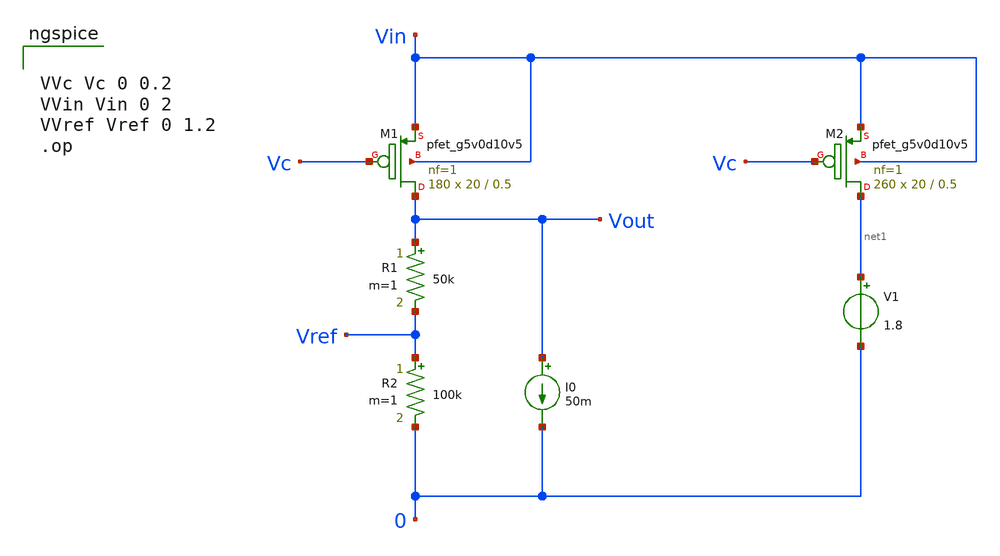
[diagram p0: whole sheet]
** sch_path: Analog_Blocks/LDO/Testbench/Pass_transistor_TB.sch
**.subckt Pass_transistor_TB
XM1 Vout Vc Vin Vin sky130_fd_pr__pfet_g5v0d10v5 L=0.5 W=20 nf=1 ad='int((1 + 1)/2) * 20 / 1 * 0.29'
+ as='int((1 + 2)/2) * 20 / 1 * 0.29' pd='2*int((1 + 1)/2) * (20 / 1 + 0.29)' ps='2*int((1 + 2)/2) * (20 / 1 + 0.29)'
+ nrd='0.29 / 20 ' nrs='0.29 / 20 ' sa=0 sb=0 sd=0 mult=180 m=180
R1 Vout Vref 50k m=1
I0 Vout 0 50m
R2 Vref 0 100k m=1
XM2 net1 Vc Vin Vin sky130_fd_pr__pfet_g5v0d10v5 L=0.5 W=20 nf=1 ad='int((1 + 1)/2) * 20 / 1 * 0.29'
+ as='int((1 + 2)/2) * 20 / 1 * 0.29' pd='2*int((1 + 1)/2) * (20 / 1 + 0.29)' ps='2*int((1 + 2)/2) * (20 / 1 + 0.29)'
+ nrd='0.29 / 20 ' nrs='0.29 / 20 ' sa=0 sb=0 sd=0 mult=260 m=260
V1 net1 0 1.8
**** begin user architecture code


VVc Vc 0 0.2
VVin Vin 0 2
VVref Vref 0 1.2
.op


**** end user architecture code
**.ends
.end
